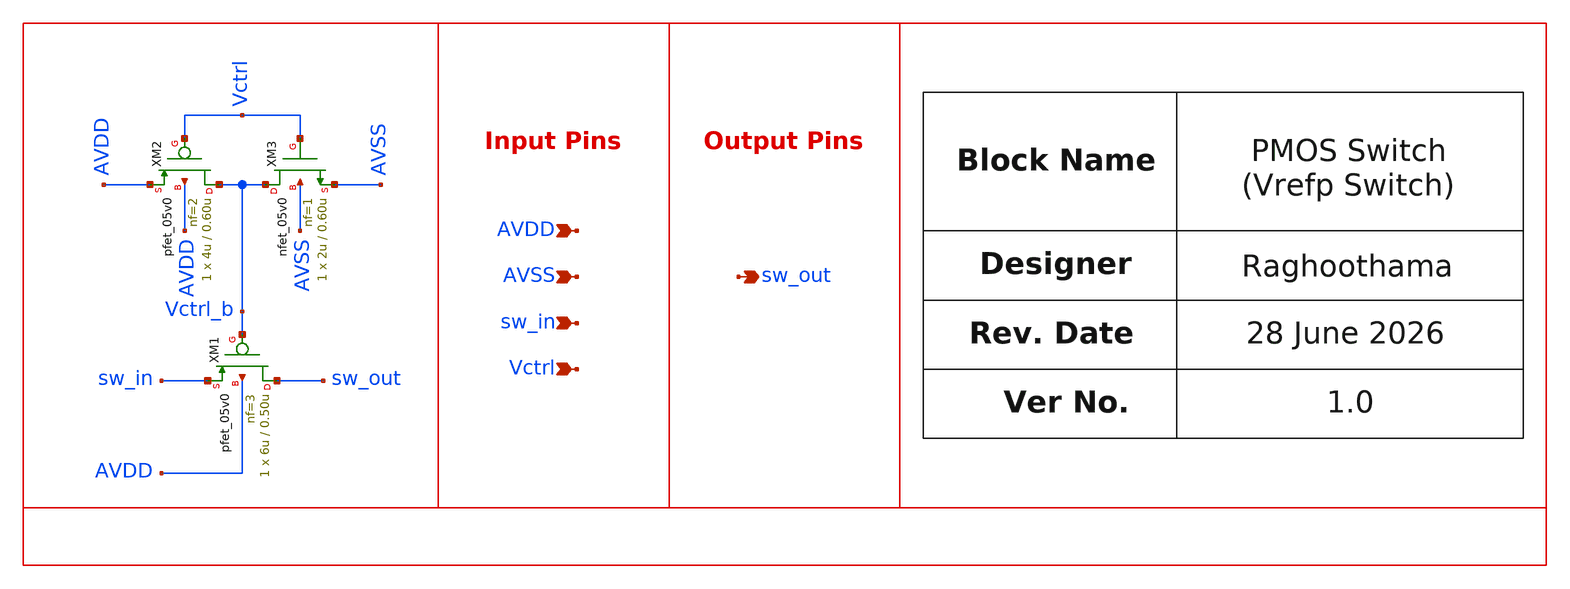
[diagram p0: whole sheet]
** sch_path: design/schematics/ADC/DSM_Loop_filter/First_int/Switches/rr_cic_bms_afe_iadc_vref_switch.sch
**.subckt rr_cic_bms_afe_iadc_vref_switch sw_in sw_out Vctrl AVSS AVDD
*.ipin sw_in
*.opin sw_out
*.ipin Vctrl
*.ipin AVSS
*.ipin AVDD
XM1 sw_out Vctrl_b sw_in AVDD pfet_05v0 L=0.50u W=6u nf=3 ad='int((nf+1)/2) * W/nf * 0.18u' as='int((nf+2)/2) * W/nf * 0.18u'
+ pd='2*int((nf+1)/2) * (W/nf + 0.18u)' ps='2*int((nf+2)/2) * (W/nf + 0.18u)' nrd='0.18u / W' nrs='0.18u / W'
+ sa=0 sb=0 sd=0 m=1
XM2 Vctrl_b Vctrl AVDD AVDD pfet_05v0 L=0.60u W=4u nf=2 ad='int((nf+1)/2) * W/nf * 0.18u' as='int((nf+2)/2) * W/nf * 0.18u'
+ pd='2*int((nf+1)/2) * (W/nf + 0.18u)' ps='2*int((nf+2)/2) * (W/nf + 0.18u)' nrd='0.18u / W' nrs='0.18u / W'
+ sa=0 sb=0 sd=0 m=1
XM3 Vctrl_b Vctrl AVSS AVSS nfet_05v0 L=0.60u W=2u nf=1 ad='int((nf+1)/2) * W/nf * 0.18u' as='int((nf+2)/2) * W/nf * 0.18u'
+ pd='2*int((nf+1)/2) * (W/nf + 0.18u)' ps='2*int((nf+2)/2) * (W/nf + 0.18u)' nrd='0.18u / W' nrs='0.18u / W'
+ sa=0 sb=0 sd=0 m=1
**.ends
.end
